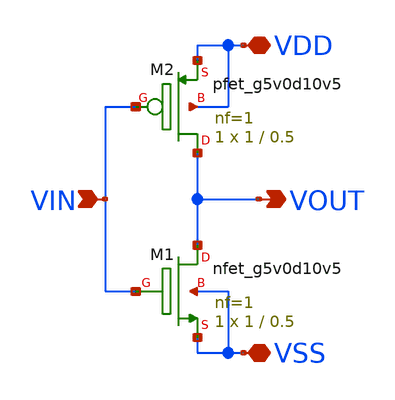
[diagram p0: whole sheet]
** sch_path: xschem/inverter.sch
**.subckt inverter VIN VOUT VDD VSS
*.ipin VIN
*.opin VOUT
*.iopin VDD
*.iopin VSS
XM1 VOUT VIN VSS VSS sky130_fd_pr__nfet_g5v0d10v5 L=0.5 W=1 nf=1 ad='int((nf+1)/2) * W/nf * 0.29' as='int((nf+2)/2) * W/nf * 0.29'
+ pd='2*int((nf+1)/2) * (W/nf + 0.29)' ps='2*int((nf+2)/2) * (W/nf + 0.29)' nrd='0.29 / W' nrs='0.29 / W'
+ sa=0 sb=0 sd=0 mult=1 m=1
XM2 VOUT VIN VDD VDD sky130_fd_pr__pfet_g5v0d10v5 L=0.5 W=1 nf=1 ad='int((nf+1)/2) * W/nf * 0.29' as='int((nf+2)/2) * W/nf * 0.29'
+ pd='2*int((nf+1)/2) * (W/nf + 0.29)' ps='2*int((nf+2)/2) * (W/nf + 0.29)' nrd='0.29 / W' nrs='0.29 / W'
+ sa=0 sb=0 sd=0 mult=1 m=1
**.ends
.end
